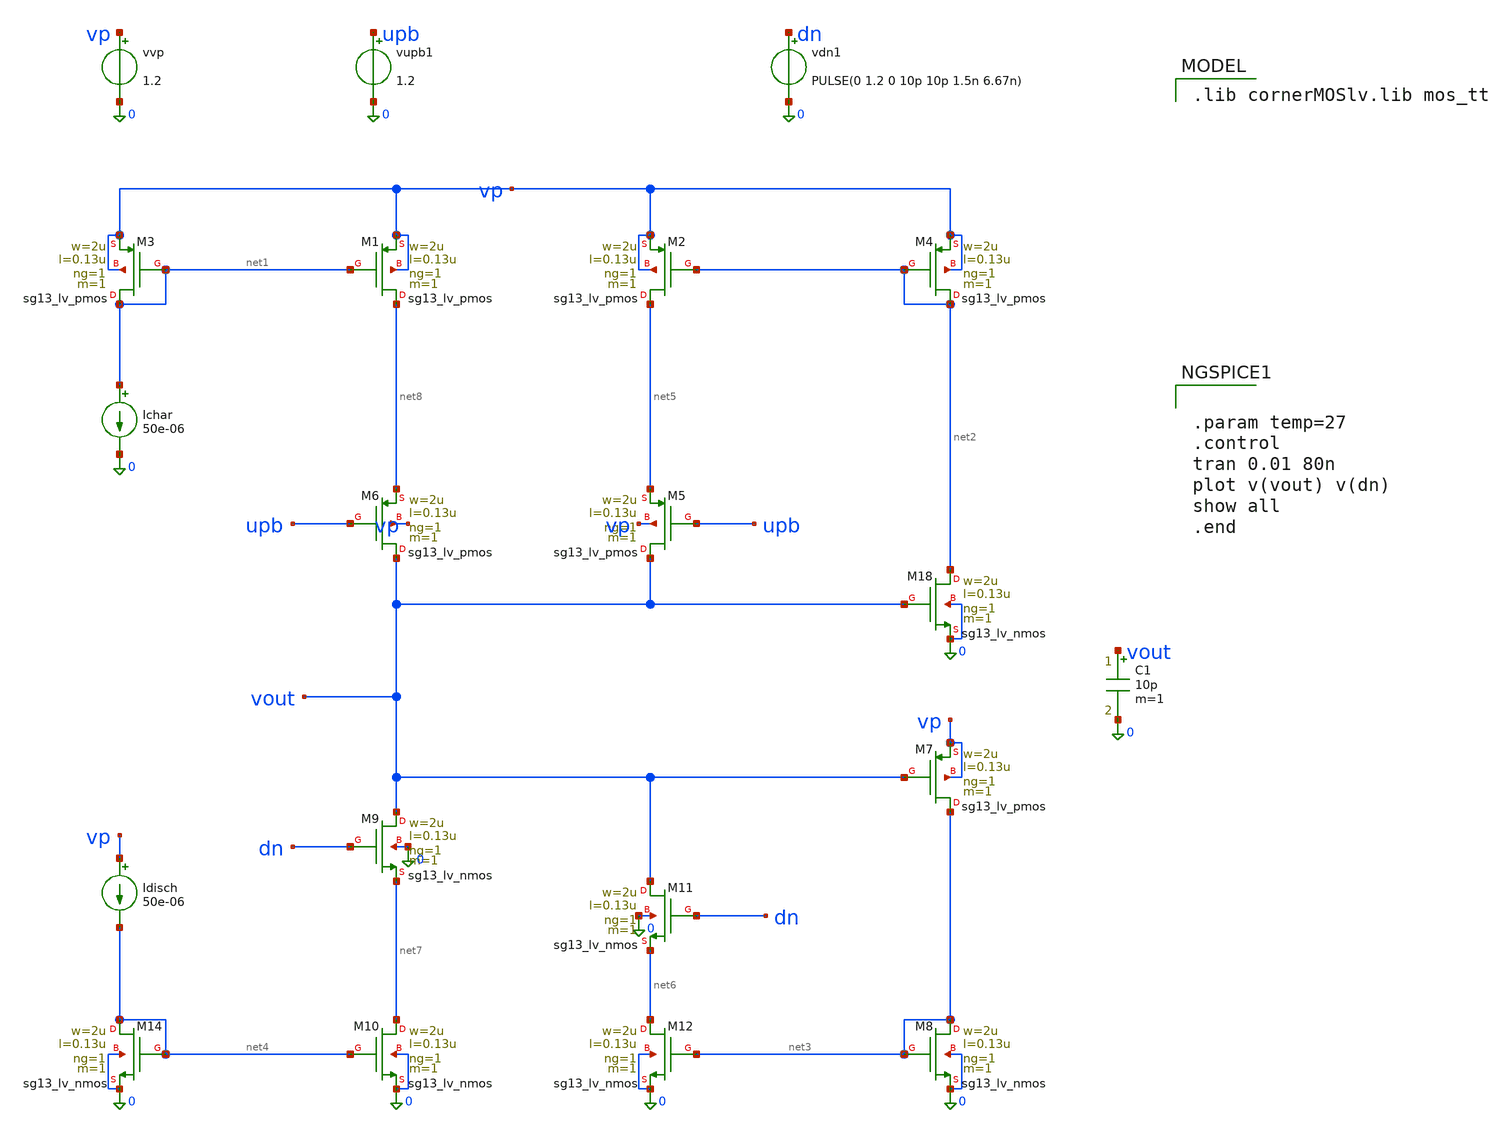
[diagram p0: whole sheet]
** sch_path: charge_pump/cp_tb/cp_v2_tb.sch
**.subckt cp_v2_tb
XM3 net1 net1 vp vp sg13_lv_pmos w=2u l=0.13u ng=1 m=1 mm_ok=1
XM1 net8 net1 vp vp sg13_lv_pmos w=2u l=0.13u ng=1 m=1 mm_ok=1
XM2 net5 net2 vp vp sg13_lv_pmos w=2u l=0.13u ng=1 m=1 mm_ok=1
XM4 net2 net2 vp vp sg13_lv_pmos w=2u l=0.13u ng=1 m=1 mm_ok=1
XM5 vout upb net5 vp sg13_lv_pmos w=2u l=0.13u ng=1 m=1 mm_ok=1
XM6 vout upb net8 vp sg13_lv_pmos w=2u l=0.13u ng=1 m=1 mm_ok=1
XM18 net2 vout 0 0 sg13_lv_nmos w=2u l=0.13u ng=1 m=1 mm_ok=1
XM7 net3 vout vp vp sg13_lv_pmos w=2u l=0.13u ng=1 m=1 mm_ok=1
XM8 net3 net3 0 0 sg13_lv_nmos w=2u l=0.13u ng=1 m=1 mm_ok=1
XM9 vout dn net7 0 sg13_lv_nmos w=2u l=0.13u ng=1 m=1 mm_ok=1
XM10 net7 net4 0 0 sg13_lv_nmos w=2u l=0.13u ng=1 m=1 mm_ok=1
XM11 vout dn net6 0 sg13_lv_nmos w=2u l=0.13u ng=1 m=1 mm_ok=1
XM12 net6 net3 0 0 sg13_lv_nmos w=2u l=0.13u ng=1 m=1 mm_ok=1
XM14 net4 net4 0 0 sg13_lv_nmos w=2u l=0.13u ng=1 m=1 mm_ok=1
Ichar net1 0 50e-06
Idisch vp net4 50e-06
C1 vout 0 10p m=1
vvp vp 0 1.2
vupb1 upb 0 1.2
vdn1 dn 0 PULSE(0 1.2 0 10p 10p 1.5n 6.67n)
**** begin user architecture code
 .lib cornerMOSlv.lib mos_tt



.param temp=27
.control
tran 0.01 80n
plot v(vout) v(dn)
show all
.end


**** end user architecture code
**.ends
.end
